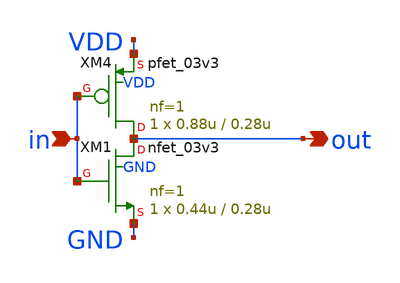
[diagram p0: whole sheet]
** sch_path: xschem_designs/inv.sch
**.subckt inv in out
*.ipin in
*.opin out
XM4 out in VDD VDD pfet_03v3 L=0.28u W=0.88u nf=1 ad='int((nf+1)/2) * W/nf * 0.18u' as='int((nf+2)/2) * W/nf * 0.18u'
+ pd='2*int((nf+1)/2) * (W/nf + 0.18u)' ps='2*int((nf+2)/2) * (W/nf + 0.18u)' nrd='0.18u / W' nrs='0.18u / W'
+ sa=0 sb=0 sd=0 m=1 par=1
XM1 out in GND GND nfet_03v3 L=0.28u W=0.44u nf=1 ad='int((nf+1)/2) * W/nf * 0.18u' as='int((nf+2)/2) * W/nf * 0.18u'
+ pd='2*int((nf+1)/2) * (W/nf + 0.18u)' ps='2*int((nf+2)/2) * (W/nf + 0.18u)' nrd='0.18u / W' nrs='0.18u / W'
+ sa=0 sb=0 sd=0 m=1 par=1
**.ends
.end
